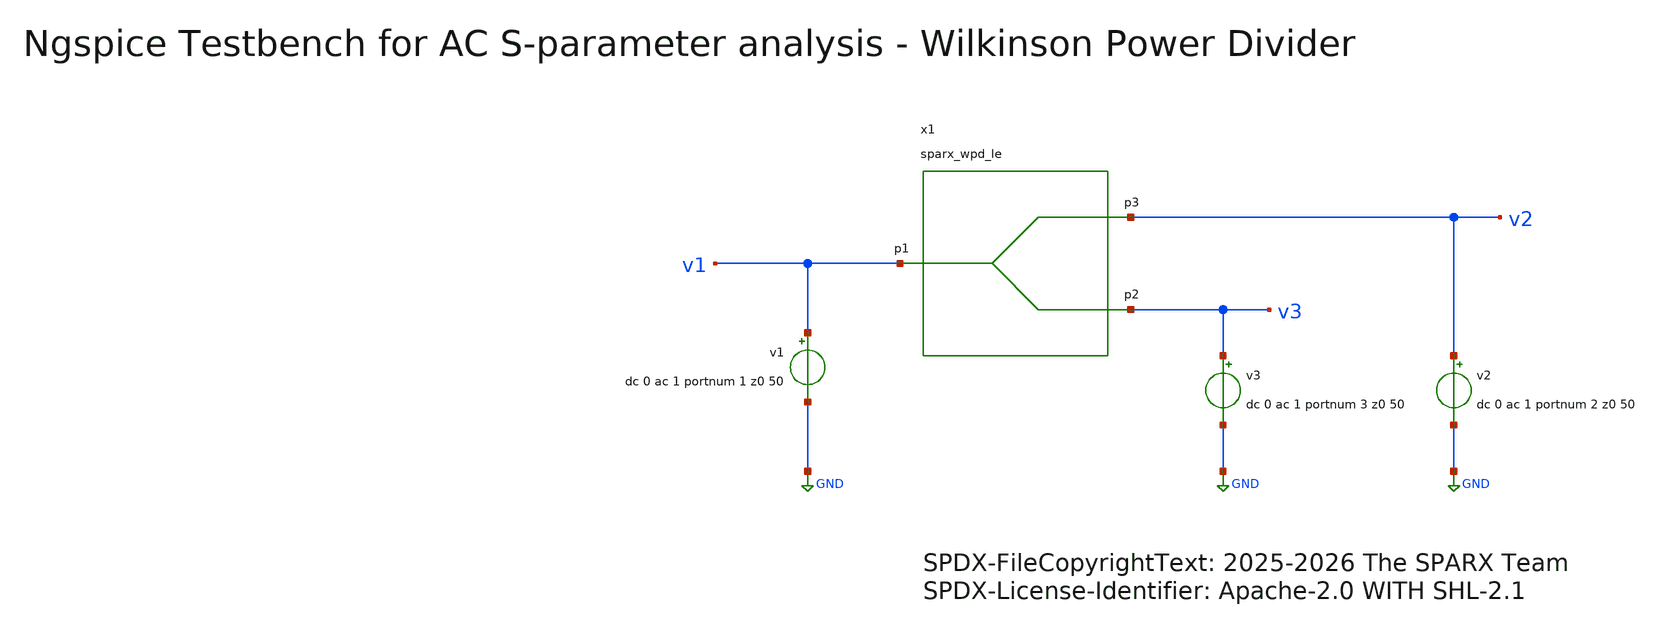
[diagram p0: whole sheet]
** sch_path: testbenches/xschem/sparx_wpd_le_tb_acsp_ngspice.sch
* SPDX-FileCopyrightText: 2025-2026 The SPARX Team
* SPDX-License-Identifier: Apache-2.0 WITH SHL-2.1
**.subckt sparx_wpd_le_tb_acsp_ngspice
v1 v1 GND dc 0 ac 1 portnum 1 z0 50
v2 v2 GND dc 0 ac 1 portnum 2 z0 50
v3 v3 GND dc 0 ac 1 portnum 3 z0 50
x1 v1 v3 v2 sparx_wpd_le
**** begin user architecture code


.include ../../../netlist/spice/sparx_wpd_le.spice
.include ../sim_range.spice
.param temp=27
.options savecurrents klu method=gear reltol=1e-3 abstol=1e-15 gmin=1e-15
.control

save all

set wr_vecnames
set wr_singlescale

* User Constants
* f_min / f_max come from ../sim_range.spice (.csparam),
* auto-synced to the loaded Touchstone by snp2le.
* edit that file for a standalone run.

* Operating Point Analysis
op
remzerovec
write @schname\.raw
set appendwrite

* AC S-Parameter Analysis
sp lin 1001 $&const.f_min $&const.f_max
remzerovec
write @schname\.raw
set appendwrite

* Calculating S-Parameters
let s11_dB = db(S_1_1)
let s21_dB = db(S_2_1)
let s12_dB = db(S_1_2)
let s22_dB = db(S_2_2)
let s33_dB = db(s_3_3)
let s31_dB = db(S_3_1)
let s13_dB = db(S_1_3)
let s32_dB = db(S_3_2)
let s23_dB = db(S_2_3)

let s11_deg = cph(S_1_1) * 180/pi
let s21_deg = cph(S_2_1) * 180/pi
let s12_deg = cph(S_1_2) * 180/pi
let s22_deg = cph(S_2_2) * 180/pi
let s33_deg = cph(s_3_3) * 180/pi
let s31_deg = cph(S_3_1) * 180/pi
let s13_deg = cph(S_1_3) * 180/pi
let s32_deg = cph(S_3_2) * 180/pi
let s23_deg = cph(S_2_3) * 180/pi

* Plotting
plot s11_dB s22_dB s33_dB
plot s11_deg s22_deg s33_deg
plot s12_dB s21_dB s13_dB s31_dB
plot s12_deg s21_deg s13_deg s31_deg
plot s23_dB s32_dB
plot s23_deg s32_deg

* Write Data
unset appendwrite
set wr_vecnames
set wr_singlescale
wrdata ../plot_simulations/data/@schname\.txt  s11_dB s22_dB s33_dB  s11_deg s22_deg s33_deg  s12_dB
+ s21_dB s13_dB s31_dB  s12_deg s21_deg s13_deg s31_deg  s23_dB s32_dB  s23_deg s32_deg

*quit
.endc



.lib cornerMOSlv.lib mos_tt
.lib cornerMOShv.lib mos_tt
.lib cornerHBT.lib hbt_typ
.lib cornerRES.lib res_typ
.lib cornerCAP.lib cap_typ
.lib cornerDIO.lib dio_tt

**** end user architecture code
**.ends
.GLOBAL GND
.end
